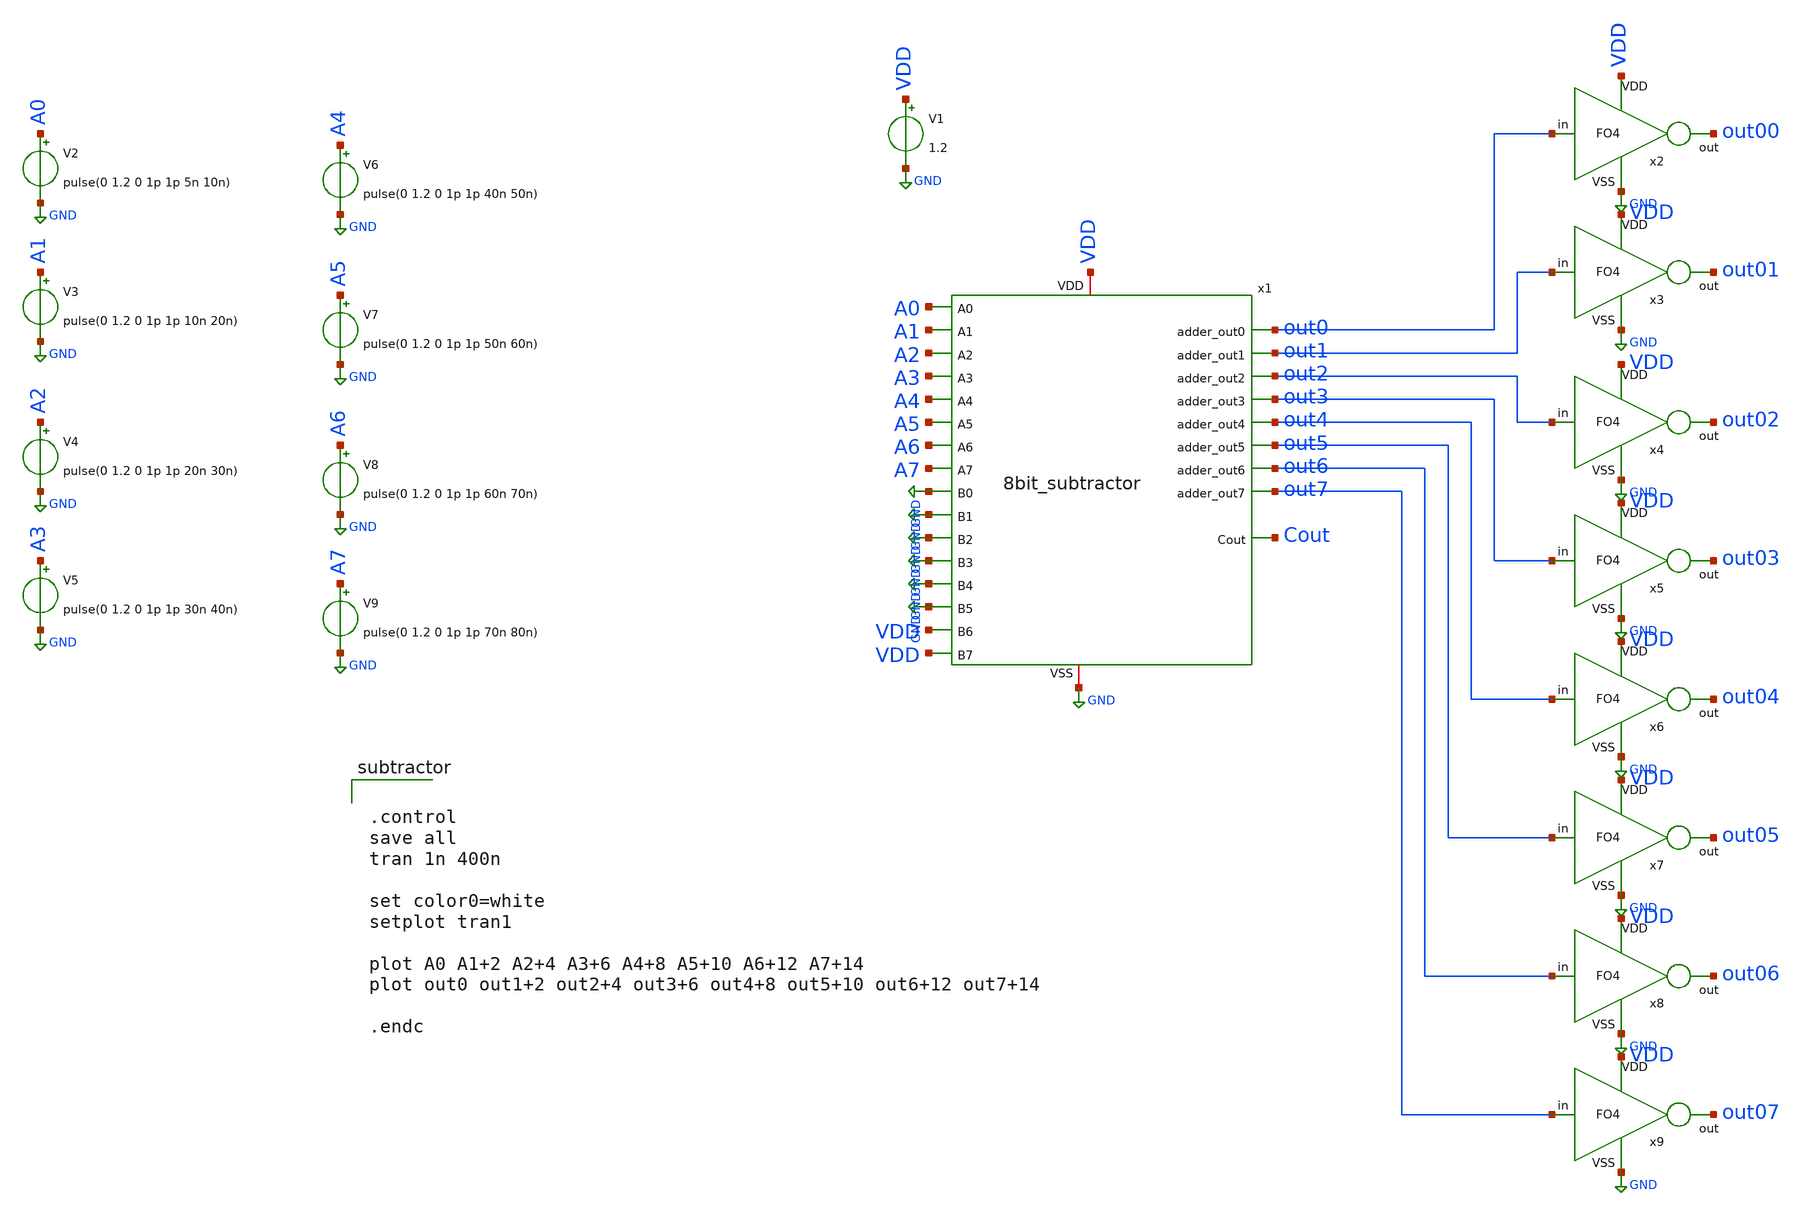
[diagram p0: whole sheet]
** sch_path: 8bit_sub_tb.sch
**.subckt 8bit_sub_tb
x1 VDD GND out7 out2 out6 out1 out3 out0 out5 out4 A0 GND Cout A1 A3 A2 A4 A7 A5 A6 GND GND GND GND
+ GND VDD VDD 8bit_subtractor
V1 VDD GND 1.2
V2 A0 GND pulse(0 1.2 0 1p 1p 5n 10n)
V3 A1 GND pulse(0 1.2 0 1p 1p 10n 20n)
V4 A2 GND pulse(0 1.2 0 1p 1p 20n 30n)
V5 A3 GND pulse(0 1.2 0 1p 1p 30n 40n)
V6 A4 GND pulse(0 1.2 0 1p 1p 40n 50n)
V7 A5 GND pulse(0 1.2 0 1p 1p 50n 60n)
V8 A6 GND pulse(0 1.2 0 1p 1p 60n 70n)
V9 A7 GND pulse(0 1.2 0 1p 1p 70n 80n)
x2 VDD GND out0 out00 FO4
x3 VDD GND out1 out01 FO4
x4 VDD GND out2 out02 FO4
x5 VDD GND out3 out03 FO4
x6 VDD GND out4 out04 FO4
x7 VDD GND out5 out05 FO4
x8 VDD GND out6 out06 FO4
x9 VDD GND out7 out07 FO4
**** begin user architecture code

** opencircuitdesign pdks install
.lib $::SKYWATER_MODELS/sky130.lib.spice tt_mm




.control
save all
tran 1n 400n

set color0=white
setplot tran1

plot A0 A1+2 A2+4 A3+6 A4+8 A5+10 A6+12 A7+14
plot out0 out1+2 out2+4 out3+6 out4+8 out5+10 out6+12 out7+14

.endc


**** end user architecture code
**.ends
.GLOBAL GND
.end
